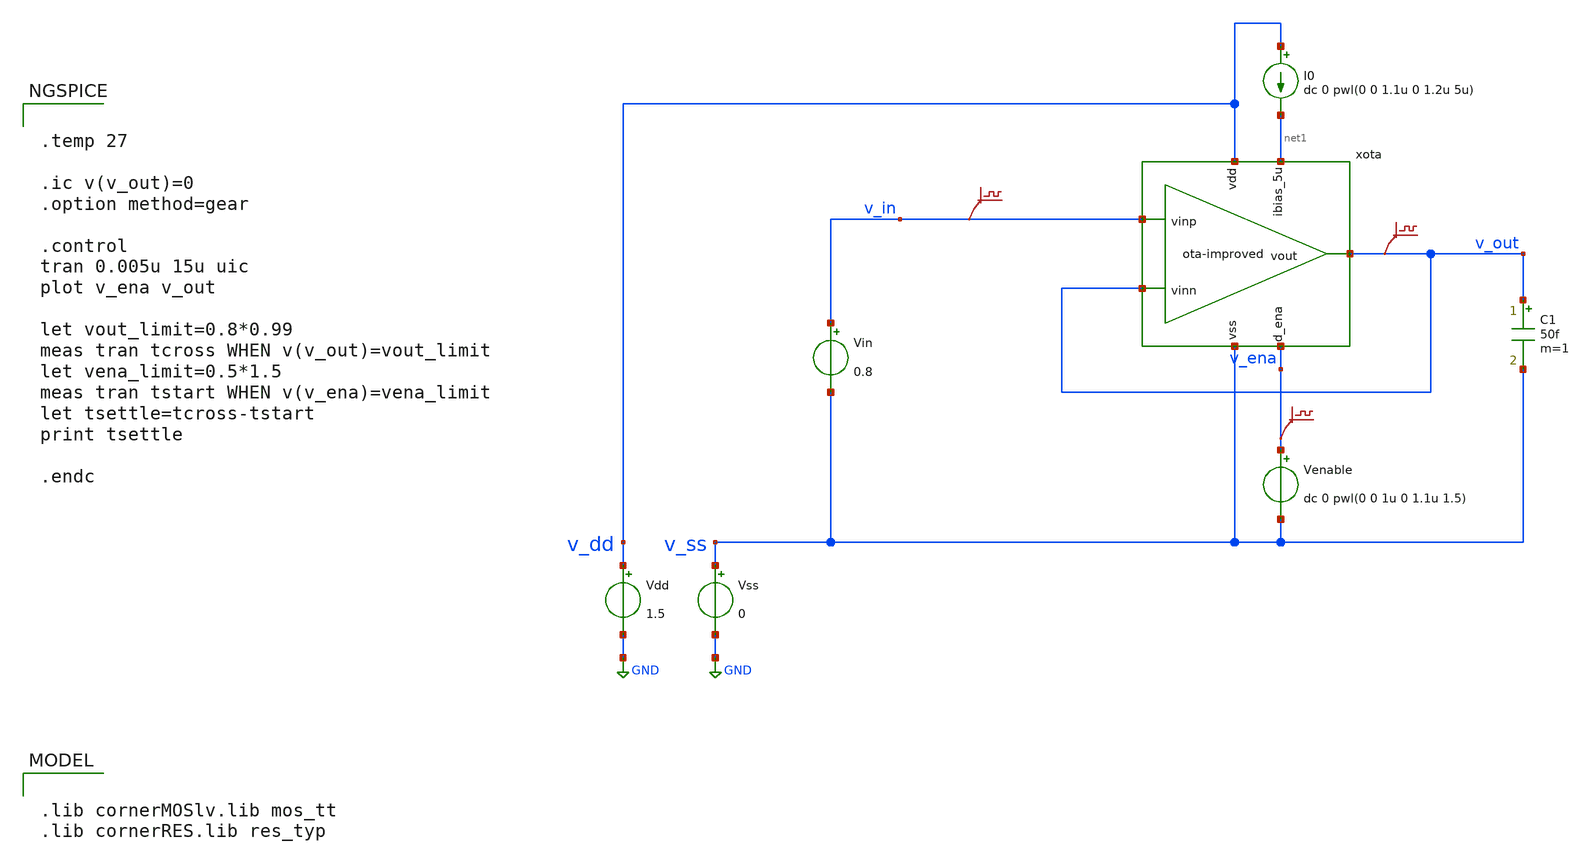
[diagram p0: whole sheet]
** sch_path: xschem/ota-improved_tb-tran.sch
* (c) 2024-2025 Harald Pretl, Apache-2.0 license
**.subckt ota-improved_tb-tran
Vdd v_dd GND 1.5
xota v_dd v_out v_in v_out net1 v_ena v_ss ota-improved
Vss v_ss GND 0
C1 v_out v_ss 50f m=1
Vin v_in v_ss 0.8
I0 v_dd net1 dc 0 pwl(0 0 1.1u 0 1.2u 5u)
Venable v_ena v_ss dc 0 pwl(0 0 1u 0 1.1u 1.5)
.save v(v_in)
.save v(v_out)
.save v(v_ena)
**** begin user architecture code


.temp 27

.ic v(v_out)=0
.option method=gear

.control
tran 0.005u 15u uic
plot v_ena v_out

let vout_limit=0.8*0.99
meas tran tcross WHEN v(v_out)=vout_limit
let vena_limit=0.5*1.5
meas tran tstart WHEN v(v_ena)=vena_limit
let tsettle=tcross-tstart
print tsettle

.endc



.lib cornerMOSlv.lib mos_tt
.lib cornerRES.lib res_typ

**** end user architecture code
**.ends

* expanding   symbol:  ota-improved.sym # of pins=7
** sym_path: xschem/ota-improved.sym
** sch_path: xschem/ota-improved.sch
.subckt ota-improved vdd vout vinp vinn ibias_5u d_ena vss
*.ipin ibias_5u
*.iopin vdd
*.iopin vss
*.ipin vinp
*.ipin vinn
*.opin vout
*.ipin d_ena
XM5 net7 gate vss vss sg13_lv_nmos w=6u l=5u ng=3 m=1 mm_ok=1
XM4 net2 gate_p vdd vdd sg13_lv_pmos w=3u l=0.5u ng=1 m=1 mm_ok=1
XM1 net5 vinp tail vss sg13_lv_nmos w=1u l=0.5u ng=1 m=1 mm_ok=1
XM2 net6 vinn tail vss sg13_lv_nmos w=1u l=0.5u ng=1 m=1 mm_ok=1
XM3 net3 gate_p vdd vdd sg13_lv_pmos w=3u l=0.5u ng=1 m=1 mm_ok=1
XM6 net1 gate vss vss sg13_lv_nmos w=2u l=5u ng=1 m=1 mm_ok=1
XMpd5 gate ena_n vss vss sg13_lv_nmos w=1u l=0.13u ng=1 m=1 mm_ok=1
XMpd3 ena ena_n vss vss sg13_lv_nmos w=1u l=0.13u ng=1 m=1 mm_ok=1
XMpd4 ena ena_n vdd vdd sg13_lv_pmos w=1u l=0.13u ng=1 m=1 mm_ok=1
XMpd6 net1 ena gate vss sg13_lv_nmos w=1u l=0.13u ng=1 m=1 mm_ok=1
XM2c vout dp_casc net6 vss sg13_lv_nmos w=1u l=0.5u ng=1 m=1 mm_ok=1
XM1c gate_p dp_casc net5 vss sg13_lv_nmos w=1u l=0.5u ng=1 m=1 mm_ok=1
XM4c vout gate_pc net2 vdd sg13_lv_pmos w=3u l=0.5u ng=1 m=1 mm_ok=1
XM3c gate_p gate_pc net3 vdd sg13_lv_pmos w=3u l=0.5u ng=1 m=1 mm_ok=1
XM7 net4 gate vss vss sg13_lv_nmos w=2u l=5u ng=1 m=1 mm_ok=1
XMpd8 gate_p ena vdd vdd sg13_lv_pmos w=1u l=0.13u ng=1 m=1 mm_ok=1
XM8_1 net8 gate_pc vdd vdd sg13_lv_pmos w=3u l=0.5u ng=1 m=1 mm_ok=1
XM9_1 net9 gate_pc vdd vdd sg13_lv_pmos w=3u l=0.5u ng=1 m=1 mm_ok=1
XMpd7 gate_pc ena vdd vdd sg13_lv_pmos w=1u l=0.13u ng=1 m=1 mm_ok=1
XM10_3 net10 dp_casc net11 vss sg13_lv_nmos w=1u l=0.5u ng=1 m=1 mm_ok=1
Vmeas gate_pc net4 0
.save i(vmeas)
Vmeas1 tail net7 0
.save i(vmeas1)
XMpd1 ena_n d_ena vss vss sg13_lv_nmos w=1u l=0.13u ng=1 m=1 mm_ok=1
XMpd2 ena_n d_ena vdd vdd sg13_lv_pmos w=1u l=0.13u ng=1 m=1 mm_ok=1
Vmeas4 ibias_5u net1 0
.save i(vmeas4)
XMpd11 vout ena_n vss vss sg13_lv_nmos w=0.5u l=0.13u ng=1 m=1 mm_ok=1
XM10_4 net11 dp_casc tail vss sg13_lv_nmos w=1u l=0.5u ng=1 m=1 mm_ok=1
XMdecoup1 vss gate vss vss sg13_lv_nmos w=8u l=1u ng=4 m=1 mm_ok=1
XMdecoup3 vdd gate_pc vdd vdd sg13_lv_pmos w=12u l=0.5u ng=4 m=1 mm_ok=1
XM10_2 net12 dp_casc net10 vss sg13_lv_nmos w=1u l=0.5u ng=1 m=1 mm_ok=1
XM10_1 dp_casc dp_casc net12 vss sg13_lv_nmos w=1u l=0.5u ng=1 m=1 mm_ok=1
XM8_2 net13 gate_pc net8 vdd sg13_lv_pmos w=3u l=0.5u ng=1 m=1 mm_ok=1
XM8_3 net14 gate_pc net13 vdd sg13_lv_pmos w=3u l=0.5u ng=1 m=1 mm_ok=1
XM9_2 net15 gate_pc net9 vdd sg13_lv_pmos w=3u l=0.5u ng=1 m=1 mm_ok=1
XM9_3 net16 gate_pc net15 vdd sg13_lv_pmos w=3u l=0.5u ng=1 m=1 mm_ok=1
XM8_4 gate_pc gate_pc net14 vdd sg13_lv_pmos w=3u l=0.5u ng=1 m=1 mm_ok=1
XM9_4 dp_casc gate_pc net16 vdd sg13_lv_pmos w=3u l=0.5u ng=1 m=1 mm_ok=1
.ends

.GLOBAL GND
.end
